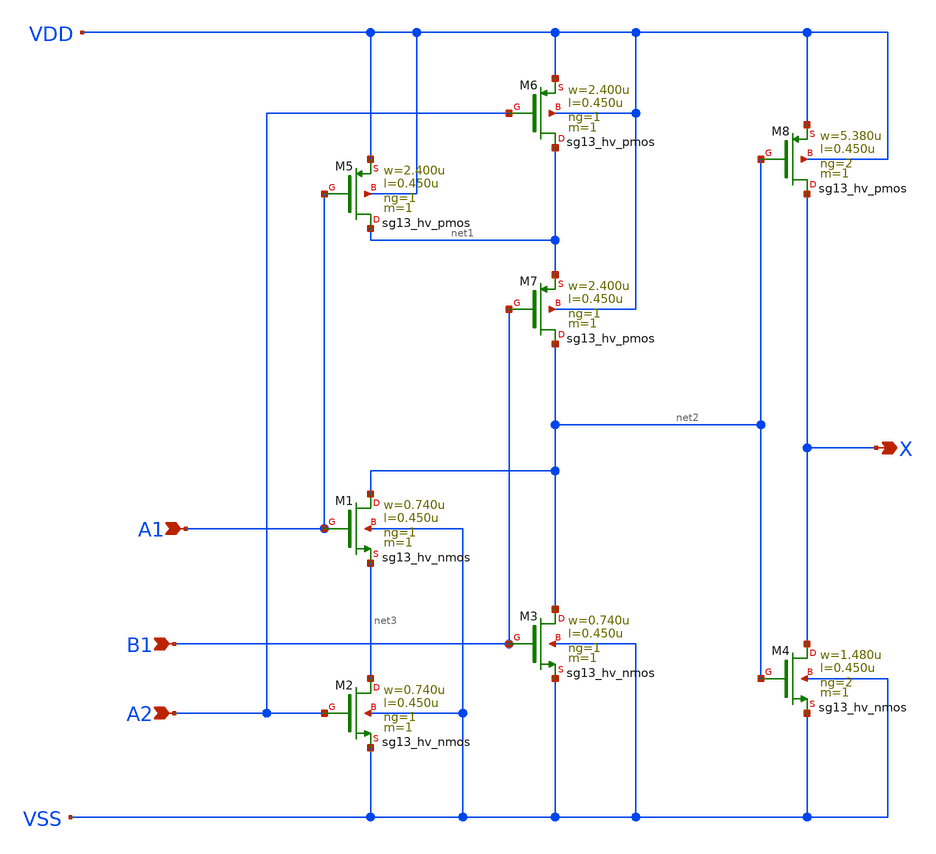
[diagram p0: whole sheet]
** sch_path: ihp-sg13g2/libs.ref/sg13g2_stdcell_hv/sch/xschem/sg13g2_hv_a21o_2.sch
**.subckt sg13g2_hv_a21o_2 X A1 A2 B1
*.opin X
*.ipin A1
*.ipin A2
*.ipin B1
XM1 net2 A1 net3 VSS sg13_hv_nmos w=0.740u l=0.450u ng=1 m=1 mm_ok=1
XM2 net3 A2 VSS VSS sg13_hv_nmos w=0.740u l=0.450u ng=1 m=1 mm_ok=1
XM3 net2 B1 VSS VSS sg13_hv_nmos w=0.740u l=0.450u ng=1 m=1 mm_ok=1
XM4 X net2 VSS VSS sg13_hv_nmos w=1.480u l=0.450u ng=2 m=1 mm_ok=1
XM5 net1 A1 VDD VDD sg13_hv_pmos w=2.400u l=0.450u ng=1 m=1 mm_ok=1
XM6 net1 A2 VDD VDD sg13_hv_pmos w=2.400u l=0.450u ng=1 m=1 mm_ok=1
XM7 net2 B1 net1 VDD sg13_hv_pmos w=2.400u l=0.450u ng=1 m=1 mm_ok=1
XM8 X net2 VDD VDD sg13_hv_pmos w=5.380u l=0.450u ng=2 m=1 mm_ok=1
**.ends
.end
